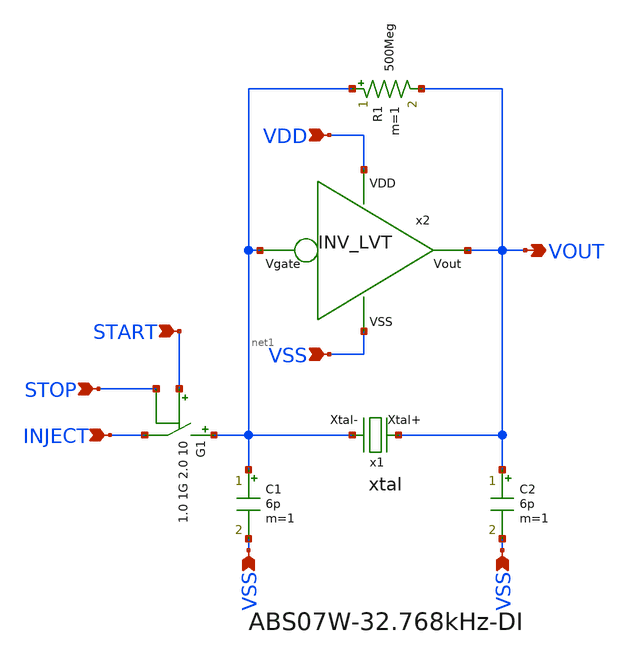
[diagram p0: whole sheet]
** sch_path: design/THESIS_EXP_RO_INVERTER_SKY130A/xtal_osc.sch
**.subckt xtal_osc VDD VSS VSS VSS VOUT INJECT STOP START
*.ipin VDD
*.ipin VSS
*.ipin VSS
*.ipin VSS
*.opin VOUT
*.ipin INJECT
*.ipin STOP
*.ipin START
x1 VOUT net1 xtal
x2 VDD net1 VOUT VSS INV_LVT
C1 net1 VSS 6p m=1
C2 VOUT VSS 6p m=1
R1 net1 VOUT 500Meg m=1
G1 net1 INJECT vcr pwl(1) START STOP 1.0 1G 2.0 10
**.ends
.end
